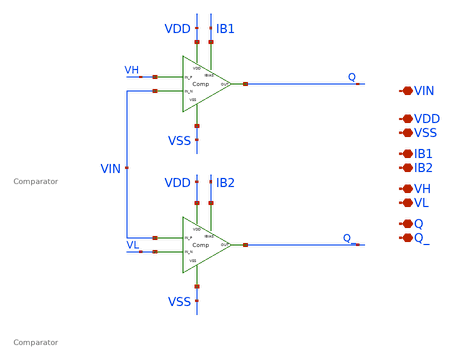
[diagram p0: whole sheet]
** sch_path: xschem/DC_DC_Converter_xschem/OTHERS/DC_DC_Converter_V7/Comparator_Pair/cmp_pair.sch
**.subckt cmp_pair VDD VSS IB1 IB2 VH VL Q Q_ VIN
*.iopin VDD
*.iopin VSS
*.iopin IB1
*.iopin IB2
*.iopin VH
*.iopin VL
*.iopin Q
*.iopin Q_
*.iopin VIN
XM1 IB1 VDD VH VIN VSS Q Comparator
XM2 IB2 VDD VIN VL VSS Q_ Comparator
**.ends

* expanding   symbol:  DC_DC_Converter/Comparator/Comparator.sym # of pins=6
** sym_path: xschem/DC_DC_Converter_xschem/OTHERS/DC_DC_Converter_V7/Comparator/Comparator.sym
** sch_path: xschem/DC_DC_Converter_xschem/OTHERS/DC_DC_Converter_V7/Comparator/Comparator.sch
.subckt Comparator IBIAS VDD IN_P IN_N VSS OUT
*.iopin VDD
*.iopin VSS
*.iopin IN_P
*.iopin IN_N
*.iopin OUT
*.iopin IBIAS
XM15 1_N IN_P IBIAS VSS sky130_fd_pr__nfet_01v8 L=1 W=5 nf=1 ad='int((nf+1)/2) * W/nf * 0.29' as='int((nf+2)/2) * W/nf * 0.29'
+ pd='2*int((nf+1)/2) * (W/nf + 0.29)' ps='2*int((nf+2)/2) * (W/nf + 0.29)' nrd='0.29 / W' nrs='0.29 / W'
+ sa=0 sb=0 sd=0 mult=1 m=1
XM1 1_P IN_N IBIAS VSS sky130_fd_pr__nfet_01v8 L=1 W=5 nf=1 ad='int((nf+1)/2) * W/nf * 0.29' as='int((nf+2)/2) * W/nf * 0.29'
+ pd='2*int((nf+1)/2) * (W/nf + 0.29)' ps='2*int((nf+2)/2) * (W/nf + 0.29)' nrd='0.29 / W' nrs='0.29 / W'
+ sa=0 sb=0 sd=0 mult=1 m=1
XM2 2_P 2_P VSS VSS sky130_fd_pr__nfet_01v8 L=2 W=2 nf=1 ad='int((nf+1)/2) * W/nf * 0.29' as='int((nf+2)/2) * W/nf * 0.29'
+ pd='2*int((nf+1)/2) * (W/nf + 0.29)' ps='2*int((nf+2)/2) * (W/nf + 0.29)' nrd='0.29 / W' nrs='0.29 / W'
+ sa=0 sb=0 sd=0 mult=1 m=1
XM10 2_N 2_P VSS VSS sky130_fd_pr__nfet_01v8 L=2 W=2 nf=1 ad='int((nf+1)/2) * W/nf * 0.29' as='int((nf+2)/2) * W/nf * 0.29'
+ pd='2*int((nf+1)/2) * (W/nf + 0.29)' ps='2*int((nf+2)/2) * (W/nf + 0.29)' nrd='0.29 / W' nrs='0.29 / W'
+ sa=0 sb=0 sd=0 mult=1 m=1
XM11 OP_1 2_N VSS VSS sky130_fd_pr__nfet_01v8 L=1 W=1 nf=1 ad='int((nf+1)/2) * W/nf * 0.29' as='int((nf+2)/2) * W/nf * 0.29'
+ pd='2*int((nf+1)/2) * (W/nf + 0.29)' ps='2*int((nf+2)/2) * (W/nf + 0.29)' nrd='0.29 / W' nrs='0.29 / W'
+ sa=0 sb=0 sd=0 mult=1 m=1
XM13 OUT OP_1 VSS VSS sky130_fd_pr__nfet_01v8 L=1 W=1 nf=1 ad='int((nf+1)/2) * W/nf * 0.29' as='int((nf+2)/2) * W/nf * 0.29'
+ pd='2*int((nf+1)/2) * (W/nf + 0.29)' ps='2*int((nf+2)/2) * (W/nf + 0.29)' nrd='0.29 / W' nrs='0.29 / W'
+ sa=0 sb=0 sd=0 mult=1 m=1
XM9 2_P 1_N VDD VDD sky130_fd_pr__pfet_01v8 L=0.5 W=1 nf=1 ad='int((nf+1)/2) * W/nf * 0.29' as='int((nf+2)/2) * W/nf * 0.29'
+ pd='2*int((nf+1)/2) * (W/nf + 0.29)' ps='2*int((nf+2)/2) * (W/nf + 0.29)' nrd='0.29 / W' nrs='0.29 / W'
+ sa=0 sb=0 sd=0 mult=1 m=1
XM6 1_N 1_N VDD VDD sky130_fd_pr__pfet_01v8 L=0.5 W=1.5 nf=1 ad='int((nf+1)/2) * W/nf * 0.29' as='int((nf+2)/2) * W/nf * 0.29'
+ pd='2*int((nf+1)/2) * (W/nf + 0.29)' ps='2*int((nf+2)/2) * (W/nf + 0.29)' nrd='0.29 / W' nrs='0.29 / W'
+ sa=0 sb=0 sd=0 mult=1 m=1
XM4 1_N 1_P VDD VDD sky130_fd_pr__pfet_01v8 L=0.5 W=1.5 nf=1 ad='int((nf+1)/2) * W/nf * 0.29' as='int((nf+2)/2) * W/nf * 0.29'
+ pd='2*int((nf+1)/2) * (W/nf + 0.29)' ps='2*int((nf+2)/2) * (W/nf + 0.29)' nrd='0.29 / W' nrs='0.29 / W'
+ sa=0 sb=0 sd=0 mult=1 m=1
XM3 1_P 1_N VDD VDD sky130_fd_pr__pfet_01v8 L=0.5 W=1.5 nf=1 ad='int((nf+1)/2) * W/nf * 0.29' as='int((nf+2)/2) * W/nf * 0.29'
+ pd='2*int((nf+1)/2) * (W/nf + 0.29)' ps='2*int((nf+2)/2) * (W/nf + 0.29)' nrd='0.29 / W' nrs='0.29 / W'
+ sa=0 sb=0 sd=0 mult=1 m=1
XM5 1_P 1_P VDD VDD sky130_fd_pr__pfet_01v8 L=0.5 W=1.5 nf=1 ad='int((nf+1)/2) * W/nf * 0.29' as='int((nf+2)/2) * W/nf * 0.29'
+ pd='2*int((nf+1)/2) * (W/nf + 0.29)' ps='2*int((nf+2)/2) * (W/nf + 0.29)' nrd='0.29 / W' nrs='0.29 / W'
+ sa=0 sb=0 sd=0 mult=1 m=1
XM7 2_N 1_P VDD VDD sky130_fd_pr__pfet_01v8 L=0.5 W=1 nf=1 ad='int((nf+1)/2) * W/nf * 0.29' as='int((nf+2)/2) * W/nf * 0.29'
+ pd='2*int((nf+1)/2) * (W/nf + 0.29)' ps='2*int((nf+2)/2) * (W/nf + 0.29)' nrd='0.29 / W' nrs='0.29 / W'
+ sa=0 sb=0 sd=0 mult=1 m=1
XM8 OP_1 2_N VDD VDD sky130_fd_pr__pfet_01v8 L=1 W=2.5 nf=1 ad='int((nf+1)/2) * W/nf * 0.29' as='int((nf+2)/2) * W/nf * 0.29'
+ pd='2*int((nf+1)/2) * (W/nf + 0.29)' ps='2*int((nf+2)/2) * (W/nf + 0.29)' nrd='0.29 / W' nrs='0.29 / W'
+ sa=0 sb=0 sd=0 mult=1 m=1
XM12 OUT OP_1 VDD VDD sky130_fd_pr__pfet_01v8 L=1 W=2.5 nf=1 ad='int((nf+1)/2) * W/nf * 0.29' as='int((nf+2)/2) * W/nf * 0.29'
+ pd='2*int((nf+1)/2) * (W/nf + 0.29)' ps='2*int((nf+2)/2) * (W/nf + 0.29)' nrd='0.29 / W' nrs='0.29 / W'
+ sa=0 sb=0 sd=0 mult=1 m=1
.ends

.end
